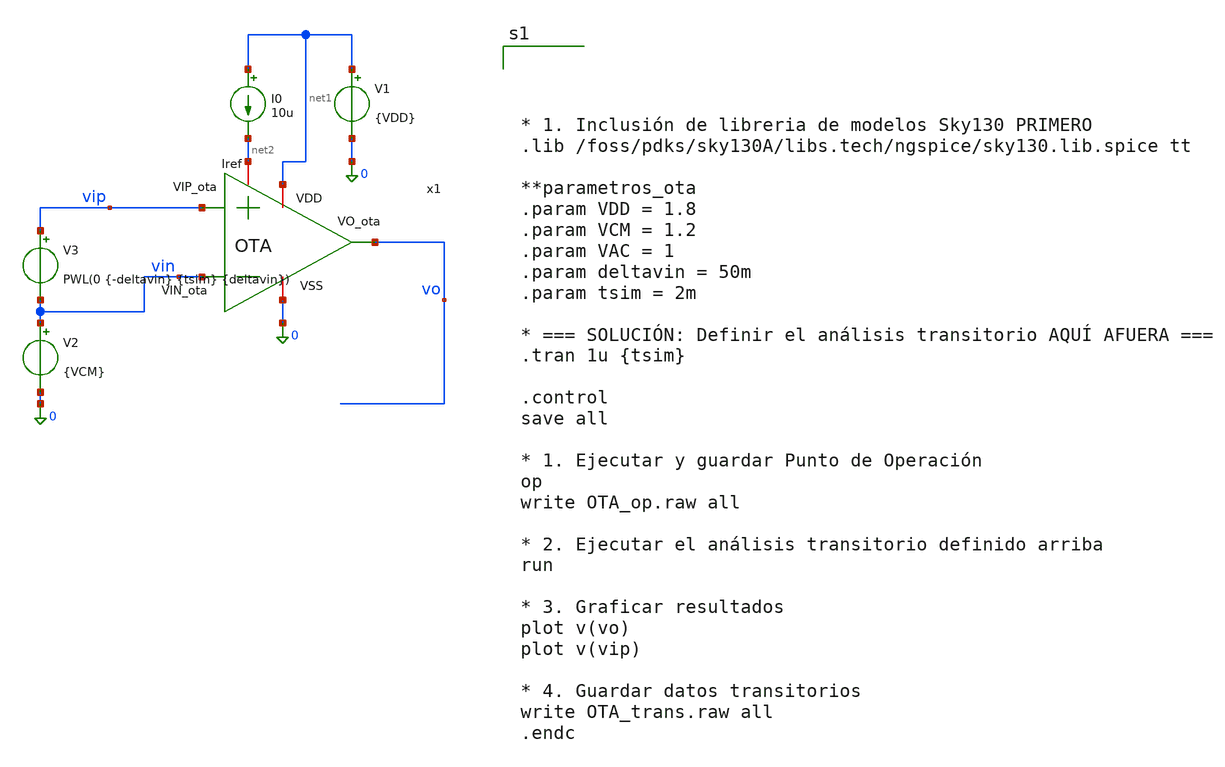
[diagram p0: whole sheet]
** sch_path: xschem/OTA_tbtran.sch
**.subckt OTA_tbtran
x1 net1 vo vin vip net2 0 OTA
V1 net1 0 {VDD}
I0 net1 net2 10u
V2 vin 0 {VCM}
V3 vip vin PWL(0 {-deltavin} {tsim} {deltavin})
**** begin user architecture code




* 1. Inclusión de libreria de modelos Sky130 PRIMERO
.lib /foss/pdks/sky130A/libs.tech/ngspice/sky130.lib.spice tt

**parametros_ota
.param VDD = 1.8
.param VCM = 1.2
.param VAC = 1
.param deltavin = 50m
.param tsim = 2m

* === SOLUCIÓN: Definir el análisis transitorio AQUÍ AFUERA ===
.tran 1u {tsim}

.control
save all

* 1. Ejecutar y guardar Punto de Operación
op
write OTA_op.raw all

* 2. Ejecutar el análisis transitorio definido arriba
run

* 3. Graficar resultados
plot v(vo)
plot v(vip)

* 4. Guardar datos transitorios
write OTA_trans.raw all
.endc



**** end user architecture code
**.ends

* expanding   symbol:  /foss/designs/LDO-sky130/xschem/OTA.sym # of pins=6
** sym_path: xschem/OTA.sym
** sch_path: xschem/OTA.sch
.subckt OTA VDD VO_ota VIN_ota VIP_ota Iref VSS
*.ipin VIN_ota
*.opin VO_ota
*.iopin Iref
*.iopin VSS
*.iopin VDD
*.ipin VIP_ota
XMr Iref Iref VSS VSS sky130_fd_pr__nfet_01v8 L=0.5 W=0.5 nf=1 ad='int((1 + 1)/2) * 0.5 / 1 * 0.29' as='int((1 + 2)/2) * 0.5 / 1 * 0.29'
+ pd='2*int((1 + 1)/2) * (0.5 / 1 + 0.29)' ps='2*int((1 + 2)/2) * (0.5 / 1 + 0.29)' nrd='0.29 / 0.5 ' nrs='0.29 / 0.5 '
+ sa=0 sb=0 sd=0 mult=1 m=1
XMo VO_ota VO_ota1 VDD VDD sky130_fd_pr__pfet_01v8 L=0.5 W=20 nf=1 ad='int((1 + 1)/2) * 20 / 1 * 0.29'
+ as='int((1 + 2)/2) * 20 / 1 * 0.29' pd='2*int((1 + 1)/2) * (20 / 1 + 0.29)' ps='2*int((1 + 2)/2) * (20 / 1 + 0.29)'
+ nrd='0.29 / 20 ' nrs='0.29 / 20 ' sa=0 sb=0 sd=0 mult=1 m=1
XMrc1 Vtail Iref VSS VSS sky130_fd_pr__nfet_01v8 L=0.5 W=2 nf=1 ad='int((1 + 1)/2) * 2 / 1 * 0.29' as='int((1 + 2)/2) * 2 / 1 * 0.29'
+ pd='2*int((1 + 1)/2) * (2 / 1 + 0.29)' ps='2*int((1 + 2)/2) * (2 / 1 + 0.29)' nrd='0.29 / 2 ' nrs='0.29 / 2 '
+ sa=0 sb=0 sd=0 mult=1 m=1
XMc2 VO_ota Iref VSS VSS sky130_fd_pr__nfet_01v8 L=0.5 W=1 nf=1 ad='int((1 + 1)/2) * 1 / 1 * 0.29' as='int((1 + 2)/2) * 1 / 1 * 0.29'
+ pd='2*int((1 + 1)/2) * (1 / 1 + 0.29)' ps='2*int((1 + 2)/2) * (1 / 1 + 0.29)' nrd='0.29 / 1 ' nrs='0.29 / 1 '
+ sa=0 sb=0 sd=0 mult=1 m=1
XMn VGP VIN_ota Vtail VSS sky130_fd_pr__nfet_01v8 L=0.5 W=40 nf=1 ad='int((1 + 1)/2) * 40 / 1 * 0.29'
+ as='int((1 + 2)/2) * 40 / 1 * 0.29' pd='2*int((1 + 1)/2) * (40 / 1 + 0.29)' ps='2*int((1 + 2)/2) * (40 / 1 + 0.29)'
+ nrd='0.29 / 40 ' nrs='0.29 / 40 ' sa=0 sb=0 sd=0 mult=1 m=1
XMp VO_ota1 VIP_ota Vtail VSS sky130_fd_pr__nfet_01v8 L=0.5 W=40 nf=1 ad='int((1 + 1)/2) * 40 / 1 * 0.29'
+ as='int((1 + 2)/2) * 40 / 1 * 0.29' pd='2*int((1 + 1)/2) * (40 / 1 + 0.29)' ps='2*int((1 + 2)/2) * (40 / 1 + 0.29)'
+ nrd='0.29 / 40 ' nrs='0.29 / 40 ' sa=0 sb=0 sd=0 mult=1 m=1
XMpr VO_ota1 VGP VDD VDD sky130_fd_pr__pfet_01v8 L=0.5 W=40 nf=1 ad='int((1 + 1)/2) * 40 / 1 * 0.29'
+ as='int((1 + 2)/2) * 40 / 1 * 0.29' pd='2*int((1 + 1)/2) * (40 / 1 + 0.29)' ps='2*int((1 + 2)/2) * (40 / 1 + 0.29)'
+ nrd='0.29 / 40 ' nrs='0.29 / 40 ' sa=0 sb=0 sd=0 mult=1 m=1
XMnr VGP VGP VDD VDD sky130_fd_pr__pfet_01v8 L=0.5 W=40 nf=1 ad='int((1 + 1)/2) * 40 / 1 * 0.29' as='int((1 + 2)/2) * 40 / 1 * 0.29'
+ pd='2*int((1 + 1)/2) * (40 / 1 + 0.29)' ps='2*int((1 + 2)/2) * (40 / 1 + 0.29)' nrd='0.29 / 40 ' nrs='0.29 / 40 '
+ sa=0 sb=0 sd=0 mult=1 m=1
XR1 VO_ota1 net1 VDD sky130_fd_pr__res_high_po W=0.35 L=360 mult=1 m=1
XC1 VO_ota net1 sky130_fd_pr__cap_mim_m3_2 W=50 L=50 MF=1 m=1
.ends

.end
